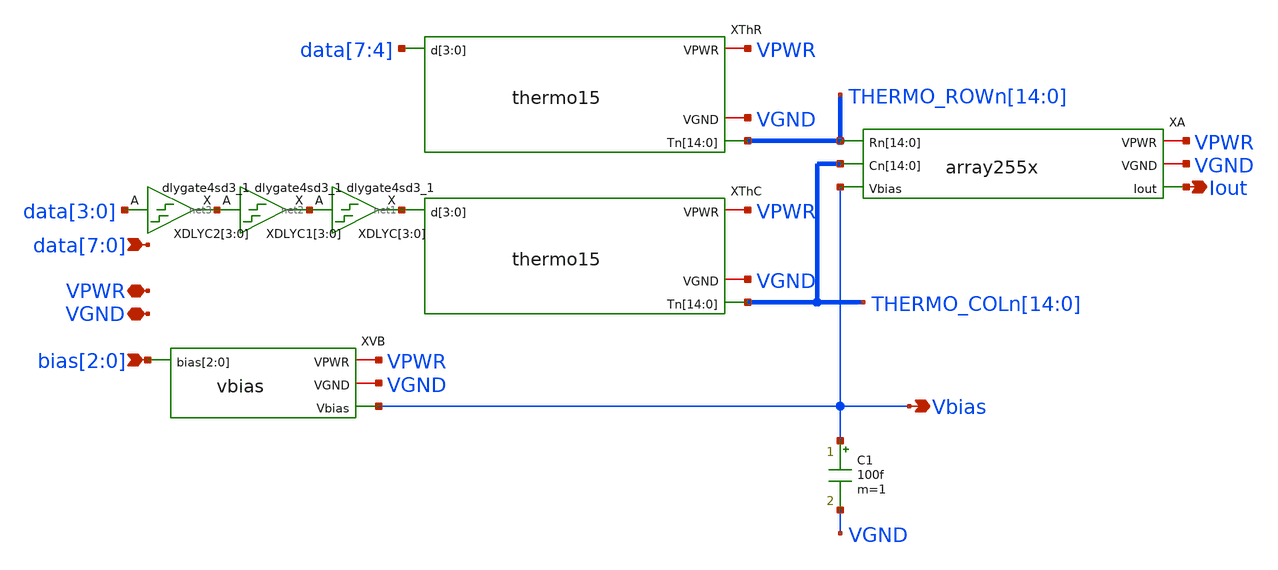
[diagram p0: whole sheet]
** sch_path: xschem/csdac255.sch
**.subckt csdac255 VPWR Iout VGND bias[2],bias[1],bias[0]
*+ data[7],data[6],data[5],data[4],data[3],data[2],data[1],data[0] Vbias
*.iopin VPWR
*.opin Iout
*.iopin VGND
*.ipin bias[2],bias[1],bias[0]
*.ipin data[7],data[6],data[5],data[4],data[3],data[2],data[1],data[0]
*.opin Vbias
XThR VPWR VGND THERMO_ROWn[14] THERMO_ROWn[13] THERMO_ROWn[12] THERMO_ROWn[11] THERMO_ROWn[10]
+ THERMO_ROWn[9] THERMO_ROWn[8] THERMO_ROWn[7] THERMO_ROWn[6] THERMO_ROWn[5] THERMO_ROWn[4] THERMO_ROWn[3]
+ THERMO_ROWn[2] THERMO_ROWn[1] THERMO_ROWn[0] data[7] data[6] data[5] data[4] thermo15
XA VPWR VGND THERMO_ROWn[14] THERMO_ROWn[13] THERMO_ROWn[12] THERMO_ROWn[11] THERMO_ROWn[10]
+ THERMO_ROWn[9] THERMO_ROWn[8] THERMO_ROWn[7] THERMO_ROWn[6] THERMO_ROWn[5] THERMO_ROWn[4] THERMO_ROWn[3]
+ THERMO_ROWn[2] THERMO_ROWn[1] THERMO_ROWn[0] THERMO_COLn[14] THERMO_COLn[13] THERMO_COLn[12] THERMO_COLn[11]
+ THERMO_COLn[10] THERMO_COLn[9] THERMO_COLn[8] THERMO_COLn[7] THERMO_COLn[6] THERMO_COLn[5] THERMO_COLn[4]
+ THERMO_COLn[3] THERMO_COLn[2] THERMO_COLn[1] THERMO_COLn[0] Vbias Iout array255x
XThC VPWR VGND THERMO_COLn[14] THERMO_COLn[13] THERMO_COLn[12] THERMO_COLn[11] THERMO_COLn[10]
+ THERMO_COLn[9] THERMO_COLn[8] THERMO_COLn[7] THERMO_COLn[6] THERMO_COLn[5] THERMO_COLn[4] THERMO_COLn[3]
+ THERMO_COLn[2] THERMO_COLn[1] THERMO_COLn[0] net1[3] net1[2] net1[1] net1[0] thermo15
XVB VPWR VGND bias[2] bias[1] bias[0] Vbias vbias
C1 Vbias VGND 100f m=1
XDLYC[3] net2[3] VGND VGND VPWR VPWR net1[3] sky130_fd_sc_hd__dlygate4sd3_1
XDLYC[2] net2[2] VGND VGND VPWR VPWR net1[2] sky130_fd_sc_hd__dlygate4sd3_1
XDLYC[1] net2[1] VGND VGND VPWR VPWR net1[1] sky130_fd_sc_hd__dlygate4sd3_1
XDLYC[0] net2[0] VGND VGND VPWR VPWR net1[0] sky130_fd_sc_hd__dlygate4sd3_1
XDLYC1[3] net3[3] VGND VGND VPWR VPWR net2[3] sky130_fd_sc_hd__dlygate4sd3_1
XDLYC1[2] net3[2] VGND VGND VPWR VPWR net2[2] sky130_fd_sc_hd__dlygate4sd3_1
XDLYC1[1] net3[1] VGND VGND VPWR VPWR net2[1] sky130_fd_sc_hd__dlygate4sd3_1
XDLYC1[0] net3[0] VGND VGND VPWR VPWR net2[0] sky130_fd_sc_hd__dlygate4sd3_1
XDLYC2[3] data[3] VGND VGND VPWR VPWR net3[3] sky130_fd_sc_hd__dlygate4sd3_1
XDLYC2[2] data[2] VGND VGND VPWR VPWR net3[2] sky130_fd_sc_hd__dlygate4sd3_1
XDLYC2[1] data[1] VGND VGND VPWR VPWR net3[1] sky130_fd_sc_hd__dlygate4sd3_1
XDLYC2[0] data[0] VGND VGND VPWR VPWR net3[0] sky130_fd_sc_hd__dlygate4sd3_1
**.ends

* expanding   symbol:  thermo15.sym # of pins=4
** sym_path: xschem/thermo15.sym
** sch_path: xschem/thermo15.sch
.subckt thermo15 VPWR VGND Tn[14] Tn[13] Tn[12] Tn[11] Tn[10] Tn[9] Tn[8] Tn[7] Tn[6] Tn[5] Tn[4]
+ Tn[3] Tn[2] Tn[1] Tn[0] d[3] d[2] d[1] d[0]
*.iopin VPWR
*.ipin d[3],d[2],d[1],d[0]
*.iopin VGND
*.opin
*+ Tn[14],Tn[13],Tn[12],Tn[11],Tn[10],Tn[9],Tn[8],Tn[7],Tn[6],Tn[5],Tn[4],Tn[3],Tn[2],Tn[1],Tn[0]
XTA2 d[1] VGND VGND VPWR VPWR TA2 sky130_fd_sc_hd__inv_1
XTBN TAN2 VGND VGND VPWR VPWR TBN sky130_fd_sc_hd__inv_2
XTA3 d[0] d[1] VGND VGND VPWR VPWR TA3 sky130_fd_sc_hd__nand2_1
XTA1 d[0] d[1] VGND VGND VPWR VPWR TA1 sky130_fd_sc_hd__nor2_1
XTAN d[2] VGND VGND VPWR VPWR TAN sky130_fd_sc_hd__inv_1
XTB1 TA1 TAN VGND VGND VPWR VPWR TB1 sky130_fd_sc_hd__nand2_1
XTB2 TA2 TAN VGND VGND VPWR VPWR TB2 sky130_fd_sc_hd__nand2_1
XTB3 TA3 TAN VGND VGND VPWR VPWR TB3 sky130_fd_sc_hd__nand2_1
XTB4 TAN VGND VGND VPWR VPWR TB4 sky130_fd_sc_hd__inv_1
XTB5 TA1 TAN VGND VGND VPWR VPWR TB5 sky130_fd_sc_hd__nor2_1
XTB6 TA2 TAN VGND VGND VPWR VPWR TB6 sky130_fd_sc_hd__nor2_1
XTB7 TA3 TAN VGND VGND VPWR VPWR TB7 sky130_fd_sc_hd__nor2_1
XOTn0 TB1 TBN VGND VGND VPWR VPWR Tn[0] sky130_fd_sc_hd__nor2_4
XOTn1 TB2 TBN VGND VGND VPWR VPWR Tn[1] sky130_fd_sc_hd__nor2_4
XOTn2 TB3 TBN VGND VGND VPWR VPWR Tn[2] sky130_fd_sc_hd__nor2_4
XOTn3 TB4 TBN VGND VGND VPWR VPWR Tn[3] sky130_fd_sc_hd__nor2_4
XOTn4 TB5 TBN VGND VGND VPWR VPWR Tn[4] sky130_fd_sc_hd__nor2_4
XOTn5 TB6 TBN VGND VGND VPWR VPWR Tn[5] sky130_fd_sc_hd__nor2_4
XOTn6 TB7 TBN VGND VGND VPWR VPWR Tn[6] sky130_fd_sc_hd__nor2_4
XOTn7 TBN VGND VGND VPWR VPWR Tn[7] sky130_fd_sc_hd__inv_4
XOTn8 TB1 TBN VGND VGND VPWR VPWR Tn[8] sky130_fd_sc_hd__nand2_4
XOTn9 TB2 TBN VGND VGND VPWR VPWR Tn[9] sky130_fd_sc_hd__nand2_4
XOTn10 TB3 TBN VGND VGND VPWR VPWR Tn[10] sky130_fd_sc_hd__nand2_4
XOTn11 TB4 TBN VGND VGND VPWR VPWR Tn[11] sky130_fd_sc_hd__nand2_4
XOTn12 TB5 TBN VGND VGND VPWR VPWR Tn[12] sky130_fd_sc_hd__nand2_4
XOTn13 TB6 TBN VGND VGND VPWR VPWR Tn[13] sky130_fd_sc_hd__nand2_4
XOTn14 TB7 TBN VGND VGND VPWR VPWR Tn[14] sky130_fd_sc_hd__nand2_4
XTAN2 d[3] VGND VGND VPWR VPWR TAN2 sky130_fd_sc_hd__inv_1
.ends


* expanding   symbol:  array255x.sym # of pins=6
** sym_path: xschem/array255x.sym
** sch_path: xschem/array255x.sch
.subckt array255x VPWR VGND Rn[14] Rn[13] Rn[12] Rn[11] Rn[10] Rn[9] Rn[8] Rn[7] Rn[6] Rn[5] Rn[4]
+ Rn[3] Rn[2] Rn[1] Rn[0] Cn[14] Cn[13] Cn[12] Cn[11] Cn[10] Cn[9] Cn[8] Cn[7] Cn[6] Cn[5] Cn[4] Cn[3]
+ Cn[2] Cn[1] Cn[0] Vbias Iout
*.iopin VPWR
*.opin Iout
*.iopin VGND
*.ipin Vbias
*.ipin
*+ Cn[14],Cn[13],Cn[12],Cn[11],Cn[10],Cn[9],Cn[8],Cn[7],Cn[6],Cn[5],Cn[4],Cn[3],Cn[2],Cn[1],Cn[0]
*.ipin
*+ Rn[14],Rn[13],Rn[12],Rn[11],Rn[10],Rn[9],Rn[8],Rn[7],Rn[6],Rn[5],Rn[4],Rn[3],Rn[2],Rn[1],Rn[0]
XIR[14] Vbias VPWR Rn[14] Rn[13] Cn[14] Cn[13] Cn[12] Cn[11] Cn[10] Cn[9] Cn[8] Cn[7] Cn[6] Cn[5]
+ Cn[4] Cn[3] Cn[2] Cn[1] Cn[0] VGND Iout row15x
XIR[13] Vbias VPWR Rn[13] Rn[12] Cn[14] Cn[13] Cn[12] Cn[11] Cn[10] Cn[9] Cn[8] Cn[7] Cn[6] Cn[5]
+ Cn[4] Cn[3] Cn[2] Cn[1] Cn[0] VGND Iout row15x
XIR[12] Vbias VPWR Rn[12] Rn[11] Cn[14] Cn[13] Cn[12] Cn[11] Cn[10] Cn[9] Cn[8] Cn[7] Cn[6] Cn[5]
+ Cn[4] Cn[3] Cn[2] Cn[1] Cn[0] VGND Iout row15x
XIR[11] Vbias VPWR Rn[11] Rn[10] Cn[14] Cn[13] Cn[12] Cn[11] Cn[10] Cn[9] Cn[8] Cn[7] Cn[6] Cn[5]
+ Cn[4] Cn[3] Cn[2] Cn[1] Cn[0] VGND Iout row15x
XIR[10] Vbias VPWR Rn[10] Rn[9] Cn[14] Cn[13] Cn[12] Cn[11] Cn[10] Cn[9] Cn[8] Cn[7] Cn[6] Cn[5]
+ Cn[4] Cn[3] Cn[2] Cn[1] Cn[0] VGND Iout row15x
XIR[9] Vbias VPWR Rn[9] Rn[8] Cn[14] Cn[13] Cn[12] Cn[11] Cn[10] Cn[9] Cn[8] Cn[7] Cn[6] Cn[5] Cn[4]
+ Cn[3] Cn[2] Cn[1] Cn[0] VGND Iout row15x
XIR[8] Vbias VPWR Rn[8] Rn[7] Cn[14] Cn[13] Cn[12] Cn[11] Cn[10] Cn[9] Cn[8] Cn[7] Cn[6] Cn[5] Cn[4]
+ Cn[3] Cn[2] Cn[1] Cn[0] VGND Iout row15x
XIR[7] Vbias VPWR Rn[7] Rn[6] Cn[14] Cn[13] Cn[12] Cn[11] Cn[10] Cn[9] Cn[8] Cn[7] Cn[6] Cn[5] Cn[4]
+ Cn[3] Cn[2] Cn[1] Cn[0] VGND Iout row15x
XIR[6] Vbias VPWR Rn[6] Rn[5] Cn[14] Cn[13] Cn[12] Cn[11] Cn[10] Cn[9] Cn[8] Cn[7] Cn[6] Cn[5] Cn[4]
+ Cn[3] Cn[2] Cn[1] Cn[0] VGND Iout row15x
XIR[5] Vbias VPWR Rn[5] Rn[4] Cn[14] Cn[13] Cn[12] Cn[11] Cn[10] Cn[9] Cn[8] Cn[7] Cn[6] Cn[5] Cn[4]
+ Cn[3] Cn[2] Cn[1] Cn[0] VGND Iout row15x
XIR[4] Vbias VPWR Rn[4] Rn[3] Cn[14] Cn[13] Cn[12] Cn[11] Cn[10] Cn[9] Cn[8] Cn[7] Cn[6] Cn[5] Cn[4]
+ Cn[3] Cn[2] Cn[1] Cn[0] VGND Iout row15x
XIR[3] Vbias VPWR Rn[3] Rn[2] Cn[14] Cn[13] Cn[12] Cn[11] Cn[10] Cn[9] Cn[8] Cn[7] Cn[6] Cn[5] Cn[4]
+ Cn[3] Cn[2] Cn[1] Cn[0] VGND Iout row15x
XIR[2] Vbias VPWR Rn[2] Rn[1] Cn[14] Cn[13] Cn[12] Cn[11] Cn[10] Cn[9] Cn[8] Cn[7] Cn[6] Cn[5] Cn[4]
+ Cn[3] Cn[2] Cn[1] Cn[0] VGND Iout row15x
XIR[1] Vbias VPWR Rn[1] Rn[0] Cn[14] Cn[13] Cn[12] Cn[11] Cn[10] Cn[9] Cn[8] Cn[7] Cn[6] Cn[5] Cn[4]
+ Cn[3] Cn[2] Cn[1] Cn[0] VGND Iout row15x
XIR[0] Vbias VPWR Rn[0] VGND Cn[14] Cn[13] Cn[12] Cn[11] Cn[10] Cn[9] Cn[8] Cn[7] Cn[6] Cn[5] Cn[4]
+ Cn[3] Cn[2] Cn[1] Cn[0] VGND Iout row15x
XIR[15] Vbias VPWR VPWR Rn[14] Cn[14] Cn[13] Cn[12] Cn[11] Cn[10] Cn[9] Cn[8] Cn[7] Cn[6] Cn[5]
+ Cn[4] Cn[3] Cn[2] Cn[1] Cn[0] VGND Iout row15x
.ends


* expanding   symbol:  vbias.sym # of pins=4
** sym_path: xschem/vbias.sym
** sch_path: xschem/vbias.sch
.subckt vbias VPWR VGND bias[2] bias[1] bias[0] Vbias
*.iopin VPWR
*.iopin VGND
*.ipin bias[2],bias[1],bias[0]
*.opin Vbias
XM1 Vbias bias[2] VPWR VPWR sky130_fd_pr__pfet_01v8 L=0.35 W=2 nf=1 ad='int((nf+1)/2) * W/nf * 0.29'
+ as='int((nf+2)/2) * W/nf * 0.29' pd='2*int((nf+1)/2) * (W/nf + 0.29)' ps='2*int((nf+2)/2) * (W/nf + 0.29)'
+ nrd='0.29 / W' nrs='0.29 / W' sa=0 sb=0 sd=0 mult=1 m=1
XM2 Vbias bias[1] VPWR VPWR sky130_fd_pr__pfet_01v8 L=0.7 W=2 nf=1 ad='int((nf+1)/2) * W/nf * 0.29' as='int((nf+2)/2) * W/nf * 0.29'
+ pd='2*int((nf+1)/2) * (W/nf + 0.29)' ps='2*int((nf+2)/2) * (W/nf + 0.29)' nrd='0.29 / W' nrs='0.29 / W'
+ sa=0 sb=0 sd=0 mult=1 m=1
XM3 Vbias bias[0] VPWR VPWR sky130_fd_pr__pfet_01v8 L=1.4 W=2 nf=1 ad='int((nf+1)/2) * W/nf * 0.29' as='int((nf+2)/2) * W/nf * 0.29'
+ pd='2*int((nf+1)/2) * (W/nf + 0.29)' ps='2*int((nf+2)/2) * (W/nf + 0.29)' nrd='0.29 / W' nrs='0.29 / W'
+ sa=0 sb=0 sd=0 mult=1 m=1
XMmirror Vbias Vbias VGND VGND sky130_fd_pr__nfet_g5v0d10v5 L=0.5 W=7.5 nf=1 ad='int((nf+1)/2) * W/nf * 0.29'
+ as='int((nf+2)/2) * W/nf * 0.29' pd='2*int((nf+1)/2) * (W/nf + 0.29)' ps='2*int((nf+2)/2) * (W/nf + 0.29)'
+ nrd='0.29 / W' nrs='0.29 / W' sa=0 sb=0 sd=0 mult=1 m=1
XM4 Vbias VGND VPWR VPWR sky130_fd_pr__pfet_01v8 L=1.4 W=2 nf=1 ad='int((nf+1)/2) * W/nf * 0.29' as='int((nf+2)/2) * W/nf * 0.29'
+ pd='2*int((nf+1)/2) * (W/nf + 0.29)' ps='2*int((nf+2)/2) * (W/nf + 0.29)' nrd='0.29 / W' nrs='0.29 / W'
+ sa=0 sb=0 sd=0 mult=1 m=1
.ends


* expanding   symbol:  row15x.sym # of pins=7
** sym_path: xschem/row15x.sym
** sch_path: xschem/row15x.sch
.subckt row15x Vbias VPWR Sn Rn Cn[14] Cn[13] Cn[12] Cn[11] Cn[10] Cn[9] Cn[8] Cn[7] Cn[6] Cn[5]
+ Cn[4] Cn[3] Cn[2] Cn[1] Cn[0] VGND Iout
*.ipin Sn
*.ipin Rn
*.ipin
*+ Cn[14],Cn[13],Cn[12],Cn[11],Cn[10],Cn[9],Cn[8],Cn[7],Cn[6],Cn[5],Cn[4],Cn[3],Cn[2],Cn[1],Cn[0]
*.iopin VPWR
*.iopin VGND
*.opin Iout
*.ipin Vbias
XIC[14] VPWR VGND Rn Cn[14] Sn Vbias Iout icell
XIC[13] VPWR VGND Rn Cn[13] Sn Vbias Iout icell
XIC[12] VPWR VGND Rn Cn[12] Sn Vbias Iout icell
XIC[11] VPWR VGND Rn Cn[11] Sn Vbias Iout icell
XIC[10] VPWR VGND Rn Cn[10] Sn Vbias Iout icell
XIC[9] VPWR VGND Rn Cn[9] Sn Vbias Iout icell
XIC[8] VPWR VGND Rn Cn[8] Sn Vbias Iout icell
XIC[7] VPWR VGND Rn Cn[7] Sn Vbias Iout icell
XIC[6] VPWR VGND Rn Cn[6] Sn Vbias Iout icell
XIC[5] VPWR VGND Rn Cn[5] Sn Vbias Iout icell
XIC[4] VPWR VGND Rn Cn[4] Sn Vbias Iout icell
XIC[3] VPWR VGND Rn Cn[3] Sn Vbias Iout icell
XIC[2] VPWR VGND Rn Cn[2] Sn Vbias Iout icell
XIC[1] VPWR VGND Rn Cn[1] Sn Vbias Iout icell
XIC[0] VPWR VGND Rn Cn[0] Sn Vbias Iout icell
XIC[15] VPWR VGND VPWR VPWR Sn Vbias Iout icell
XIC_dummy_left VPWR VGND VPWR VPWR VPWR VGND net1 icell
XIC_dummy_right VPWR VGND VPWR VPWR VPWR VGND net2 icell
.ends


* expanding   symbol:  icell.sym # of pins=7
** sym_path: xschem/icell.sym
** sch_path: xschem/icell.sch
.subckt icell VPWR VGND Rn Cn Sn Vbias Iout
*.ipin Rn
*.iopin VPWR
*.opin Iout
*.iopin VGND
*.ipin Cn
*.ipin Sn
*.ipin Vbias
XM2 Ien Sn VPWR VPWR sky130_fd_pr__pfet_01v8 L=0.15 W=0.5 nf=1 ad='int((nf+1)/2) * W/nf * 0.29' as='int((nf+2)/2) * W/nf * 0.29'
+ pd='2*int((nf+1)/2) * (W/nf + 0.29)' ps='2*int((nf+2)/2) * (W/nf + 0.29)' nrd='0.29 / W' nrs='0.29 / W'
+ sa=0 sb=0 sd=0 mult=1 m=1
XM3 Ien Sn PDM VGND sky130_fd_pr__nfet_01v8 L=0.15 W=0.5 nf=1 ad='int((nf+1)/2) * W/nf * 0.29' as='int((nf+2)/2) * W/nf * 0.29'
+ pd='2*int((nf+1)/2) * (W/nf + 0.29)' ps='2*int((nf+2)/2) * (W/nf + 0.29)' nrd='0.29 / W' nrs='0.29 / W'
+ sa=0 sb=0 sd=0 mult=1 m=1
XM4 Ien Cn PUM VPWR sky130_fd_pr__pfet_01v8 L=0.15 W=0.5 nf=1 ad='int((nf+1)/2) * W/nf * 0.29' as='int((nf+2)/2) * W/nf * 0.29'
+ pd='2*int((nf+1)/2) * (W/nf + 0.29)' ps='2*int((nf+2)/2) * (W/nf + 0.29)' nrd='0.29 / W' nrs='0.29 / W'
+ sa=0 sb=0 sd=0 mult=1 m=1
XM5 PUM Rn VPWR VPWR sky130_fd_pr__pfet_01v8 L=0.15 W=0.5 nf=1 ad='int((nf+1)/2) * W/nf * 0.29' as='int((nf+2)/2) * W/nf * 0.29'
+ pd='2*int((nf+1)/2) * (W/nf + 0.29)' ps='2*int((nf+2)/2) * (W/nf + 0.29)' nrd='0.29 / W' nrs='0.29 / W'
+ sa=0 sb=0 sd=0 mult=1 m=1
XM6 PDM Rn VGND VGND sky130_fd_pr__nfet_01v8 L=0.15 W=0.5 nf=1 ad='int((nf+1)/2) * W/nf * 0.29' as='int((nf+2)/2) * W/nf * 0.29'
+ pd='2*int((nf+1)/2) * (W/nf + 0.29)' ps='2*int((nf+2)/2) * (W/nf + 0.29)' nrd='0.29 / W' nrs='0.29 / W'
+ sa=0 sb=0 sd=0 mult=1 m=1
XM7 PDM Cn VGND VGND sky130_fd_pr__nfet_01v8 L=0.15 W=0.5 nf=1 ad='int((nf+1)/2) * W/nf * 0.29' as='int((nf+2)/2) * W/nf * 0.29'
+ pd='2*int((nf+1)/2) * (W/nf + 0.29)' ps='2*int((nf+2)/2) * (W/nf + 0.29)' nrd='0.29 / W' nrs='0.29 / W'
+ sa=0 sb=0 sd=0 mult=1 m=1
XM1 SM Vbias VGND VGND sky130_fd_pr__nfet_g5v0d10v5 L=0.5 W=0.5 nf=1 ad='int((nf+1)/2) * W/nf * 0.29'
+ as='int((nf+2)/2) * W/nf * 0.29' pd='2*int((nf+1)/2) * (W/nf + 0.29)' ps='2*int((nf+2)/2) * (W/nf + 0.29)'
+ nrd='0.29 / W' nrs='0.29 / W' sa=0 sb=0 sd=0 mult=1 m=1
XM8 Iout Ien SM VGND sky130_fd_pr__nfet_g5v0d10v5 L=0.5 W=1.0 nf=1 ad='int((nf+1)/2) * W/nf * 0.29' as='int((nf+2)/2) * W/nf * 0.29'
+ pd='2*int((nf+1)/2) * (W/nf + 0.29)' ps='2*int((nf+2)/2) * (W/nf + 0.29)' nrd='0.29 / W' nrs='0.29 / W'
+ sa=0 sb=0 sd=0 mult=1 m=1
.ends

.end
